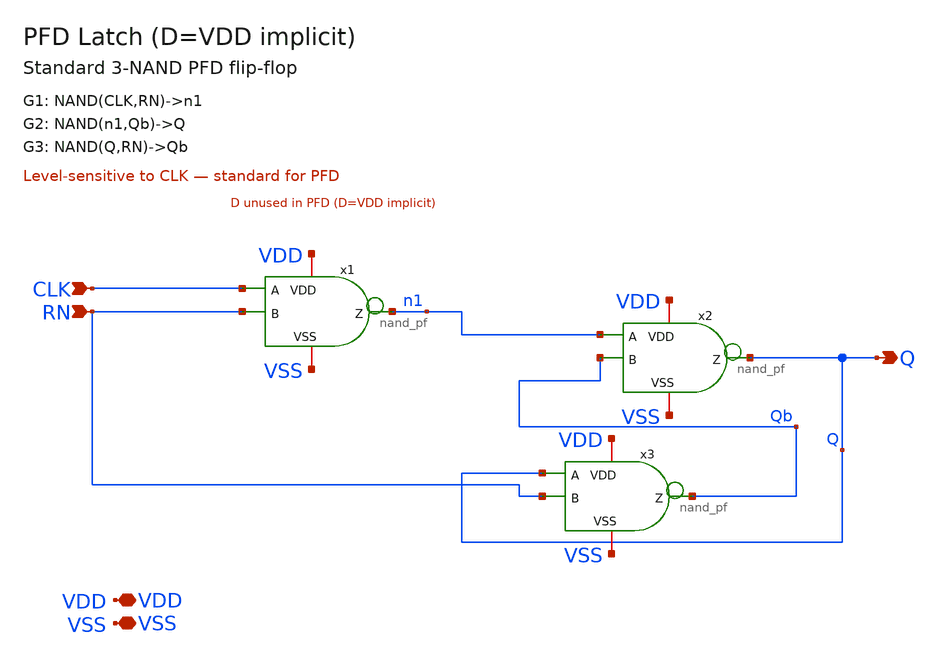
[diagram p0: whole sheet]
** sch_path: designs/libs/PDF/dff_resetn.sch
**.subckt dff_resetn CLK RN Q VDD VSS
*.ipin CLK
*.ipin RN
*.opin Q
*.iopin VDD
*.iopin VSS
x1 VDD n1 CLK RN VSS nand_pf
x2 VDD Q n1 Qb VSS nand_pf
x3 VDD Qb Q RN VSS nand_pf
**.ends
.end
